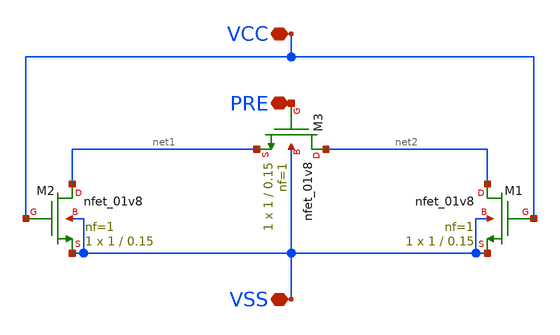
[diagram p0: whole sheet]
** sch_path: peripherals/precharge.sch
**.subckt precharge VSS VCC PRE
*.iopin VSS
*.iopin VCC
*.iopin PRE
XM2 net1 VCC VSS VSS sky130_fd_pr__nfet_01v8 L=0.15 W=1 nf=1 ad='int((1 + 1)/2) * 1 / 1 * 0.29' as='int((1 + 2)/2) * 1 / 1 * 0.29'
+ pd='2*int((1 + 1)/2) * (1 / 1 + 0.29)' ps='2*int((1 + 2)/2) * (1 / 1 + 0.29)' nrd='0.29 / 1 ' nrs='0.29 / 1 '
+ sa=0 sb=0 sd=0 mult=1 m=1
XM1 net2 VCC VSS VSS sky130_fd_pr__nfet_01v8 L=0.15 W=1 nf=1 ad='int((1 + 1)/2) * 1 / 1 * 0.29' as='int((1 + 2)/2) * 1 / 1 * 0.29'
+ pd='2*int((1 + 1)/2) * (1 / 1 + 0.29)' ps='2*int((1 + 2)/2) * (1 / 1 + 0.29)' nrd='0.29 / 1 ' nrs='0.29 / 1 '
+ sa=0 sb=0 sd=0 mult=1 m=1
XM3 net2 PRE net1 VSS sky130_fd_pr__nfet_01v8 L=0.15 W=1 nf=1 ad='int((1 + 1)/2) * 1 / 1 * 0.29' as='int((1 + 2)/2) * 1 / 1 * 0.29'
+ pd='2*int((1 + 1)/2) * (1 / 1 + 0.29)' ps='2*int((1 + 2)/2) * (1 / 1 + 0.29)' nrd='0.29 / 1 ' nrs='0.29 / 1 '
+ sa=0 sb=0 sd=0 mult=1 m=1
**.ends
.end
